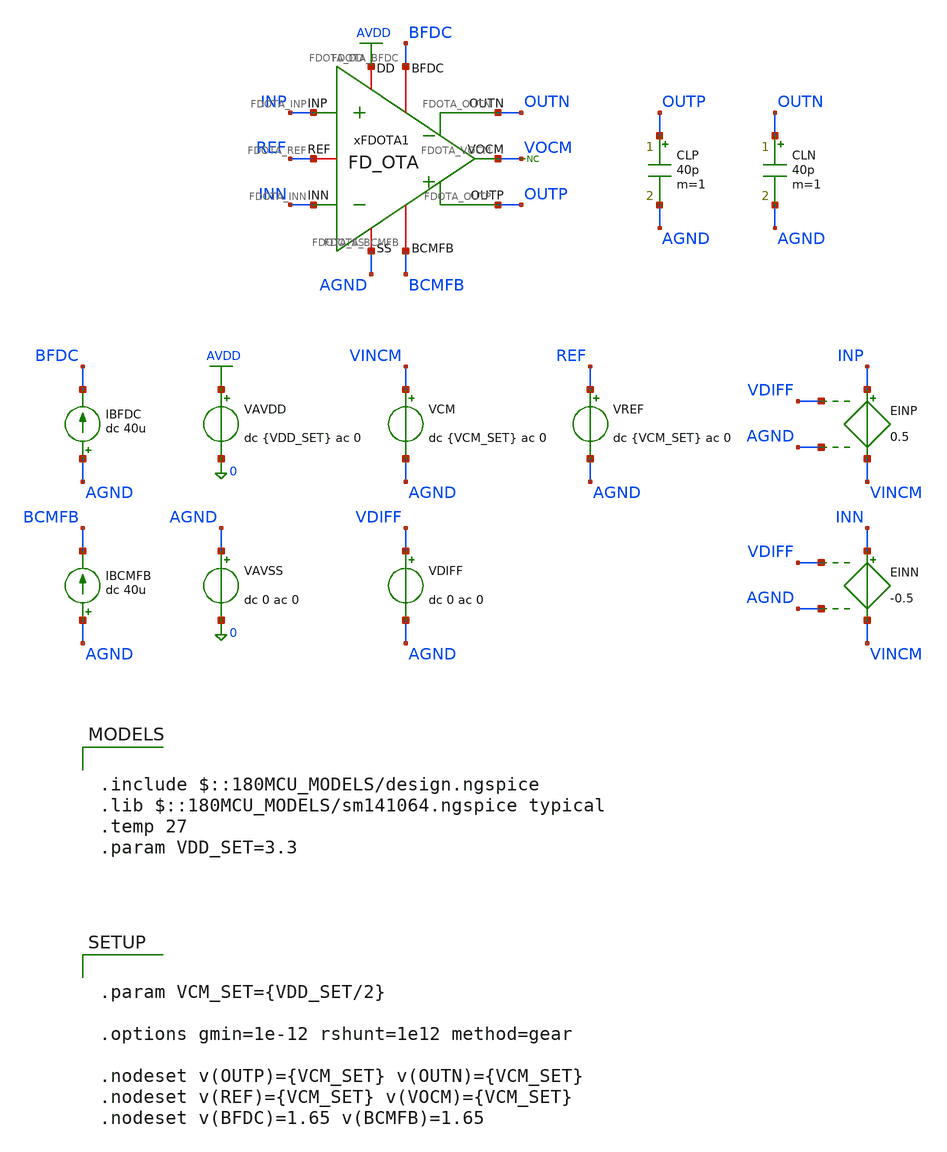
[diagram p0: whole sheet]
** sch_path: Design_Files/IC Design/Testbench/FD_OTA/FDOTA old/FD_OTA_TB_OL_NOM.sch
**.subckt FD_OTA_TB_OL_NOM
IBFDC AGND BFDC dc 40u
VAVDD AVDD 0 dc {VDD_SET} ac 0
.save i(vavdd)
VCM VINCM AGND dc {VCM_SET} ac 0
VDIFF VDIFF AGND dc 0 ac 0
VAVSS AGND 0 dc 0 ac 0
.save i(vavss)
VREF REF AGND dc {VCM_SET} ac 0
EINP INP VINCM VDIFF AGND 0.5
EINN INN VINCM VDIFF AGND -0.5
IBCMFB AGND BCMFB dc 40u
CLP OUTP AGND 40p m=1
CLN OUTN AGND 40p m=1
* noconn VOCM
xFDOTA1 AVDD AGND INP INN OUTN BFDC OUTP BCMFB REF VOCM FD_OTA
**** begin user architecture code

.include $::180MCU_MODELS/design.ngspice
.lib $::180MCU_MODELS/sm141064.ngspice typical
.temp 27
.param VDD_SET=3.3




.control
destroy all
save all
set wr_vecnames
set wr_singlescale
option numdgt=15

shell mkdir -p
+ /foss/designs/ECG_Acquisition_IC/Measurement_Results/IC_Simulation/FD_OTA/FDOTA/NOM.Result_txt

shell rm -f
+ /foss/designs/ECG_Acquisition_IC/Measurement_Results/IC_Simulation/FD_OTA/FDOTA/NOM.Result_txt/NOM.ol_op.txt
shell rm -f
+ /foss/designs/ECG_Acquisition_IC/Measurement_Results/IC_Simulation/FD_OTA/FDOTA/NOM.Result_txt/NOM.ol_diff_ac.txt
shell rm -f
+ /foss/designs/ECG_Acquisition_IC/Measurement_Results/IC_Simulation/FD_OTA/FDOTA/NOM.Result_txt/NOM.ol_cm_ac.txt
shell rm -f
+ /foss/designs/ECG_Acquisition_IC/Measurement_Results/IC_Simulation/FD_OTA/FDOTA/NOM.Result_txt/NOM.ol_psrrp_ac.txt
shell rm -f
+ /foss/designs/ECG_Acquisition_IC/Measurement_Results/IC_Simulation/FD_OTA/FDOTA/NOM.Result_txt/NOM.ol_psrrn_ac.txt
shell rm -f
+ /foss/designs/ECG_Acquisition_IC/Measurement_Results/IC_Simulation/FD_OTA/FDOTA/NOM.Result_txt/NOM.ol_vtc.txt

* OP
op

let voutcm = 0.5*(v(OUTP)+v(OUTN))
let voutdiff = v(OUTP)-v(OUTN)
let idd = -vavdd#branch
let ibias_fdc = 40u + 0*v(AVDD)
let ibias_cmfb = 40u + 0*v(AVDD)

wrdata
+ /foss/designs/ECG_Acquisition_IC/Measurement_Results/IC_Simulation/FD_OTA/FDOTA/NOM.Result_txt/NOM.ol_op.txt v(AVDD) v(INP) v(INN) v(OUTP) v(OUTN) voutcm voutdiff v(REF) v(VOCM) v(BFDC) v(BCMFB) idd ibias_fdc
+ ibias_cmfb

* Diff AC
alter @VCM[ACMAG] = 0
alter @VDIFF[ACMAG] = 1
alter @VDIFF[ACPHASE] = 0
alter @VREF[ACMAG] = 0
alter @VAVDD[ACMAG] = 0
alter @VAVSS[ACMAG] = 0

ac dec 200 0.01 100G

let vin_diff = v(INP)-v(INN)
let voutdiff = v(OUTP)-v(OUTN)
let vin_diff_real = real(vin_diff)
let vin_diff_imag = imag(vin_diff)
let voutdiff_real = real(voutdiff)
let voutdiff_imag = imag(voutdiff)

setscale frequency

wrdata
+ /foss/designs/ECG_Acquisition_IC/Measurement_Results/IC_Simulation/FD_OTA/FDOTA/NOM.Result_txt/NOM.ol_diff_ac.txt vin_diff_real vin_diff_imag voutdiff_real voutdiff_imag

* CM AC
alter @VCM[ACMAG] = 1
alter @VCM[ACPHASE] = 0
alter @VDIFF[ACMAG] = 0
alter @VREF[ACMAG] = 0
alter @VAVDD[ACMAG] = 0
alter @VAVSS[ACMAG] = 0

ac dec 200 0.01 100G

let vin_cm = 0.5*(v(INP)+v(INN))
let voutdiff = v(OUTP)-v(OUTN)
let vin_cm_real = real(vin_cm)
let vin_cm_imag = imag(vin_cm)
let voutdiff_real = real(voutdiff)
let voutdiff_imag = imag(voutdiff)

setscale frequency

wrdata
+ /foss/designs/ECG_Acquisition_IC/Measurement_Results/IC_Simulation/FD_OTA/FDOTA/NOM.Result_txt/NOM.ol_cm_ac.txt vin_cm_real vin_cm_imag voutdiff_real voutdiff_imag

* PSRR+
alter @VCM[ACMAG] = 0
alter @VDIFF[ACMAG] = 0
alter @VREF[ACMAG] = 0
alter @VAVDD[ACMAG] = 1
alter @VAVDD[ACPHASE] = 0
alter @VAVSS[ACMAG] = 0

ac dec 200 0.01 100G

let vavdd_ac = v(AVDD)
let voutdiff = v(OUTP)-v(OUTN)
let vavdd_real = real(vavdd_ac)
let vavdd_imag = imag(vavdd_ac)
let voutdiff_real = real(voutdiff)
let voutdiff_imag = imag(voutdiff)

setscale frequency

wrdata
+ /foss/designs/ECG_Acquisition_IC/Measurement_Results/IC_Simulation/FD_OTA/FDOTA/NOM.Result_txt/NOM.ol_psrrp_ac.txt vavdd_real vavdd_imag voutdiff_real voutdiff_imag

* PSRR-
alter @VCM[ACMAG] = 0
alter @VDIFF[ACMAG] = 0
alter @VREF[ACMAG] = 0
alter @VAVDD[ACMAG] = 0
alter @VAVSS[ACMAG] = 1
alter @VAVSS[ACPHASE] = 0

ac dec 200 0.01 100G

let vagnd_ac = v(AGND)
let voutdiff = v(OUTP)-v(OUTN)
let vagnd_real = real(vagnd_ac)
let vagnd_imag = imag(vagnd_ac)
let voutdiff_real = real(voutdiff)
let voutdiff_imag = imag(voutdiff)

setscale frequency

wrdata
+ /foss/designs/ECG_Acquisition_IC/Measurement_Results/IC_Simulation/FD_OTA/FDOTA/NOM.Result_txt/NOM.ol_psrrn_ac.txt vagnd_real vagnd_imag voutdiff_real voutdiff_imag

* VTC
alter @VCM[ACMAG] = 0
alter @VDIFF[ACMAG] = 0
alter @VREF[ACMAG] = 0
alter @VAVDD[ACMAG] = 0
alter @VAVSS[ACMAG] = 0

dc VDIFF -20m 20m 10u

let vin_diff = v(INP)-v(INN)
let voutcm = 0.5*(v(OUTP)+v(OUTN))
let voutdiff = v(OUTP)-v(OUTN)
let idd = -vavdd#branch

setscale vin_diff

wrdata
+ /foss/designs/ECG_Acquisition_IC/Measurement_Results/IC_Simulation/FD_OTA/FDOTA/NOM.Result_txt/NOM.ol_vtc.txt v(INP) v(INN) v(OUTP) v(OUTN) voutcm voutdiff v(VOCM) idd

quit
.endc




.param VCM_SET={VDD_SET/2}

.options gmin=1e-12 rshunt=1e12 method=gear

.nodeset v(OUTP)={VCM_SET} v(OUTN)={VCM_SET}
.nodeset v(REF)={VCM_SET} v(VOCM)={VCM_SET}
.nodeset v(BFDC)=1.65 v(BCMFB)=1.65


**** end user architecture code
**.ends
.GLOBAL AVDD
.end
